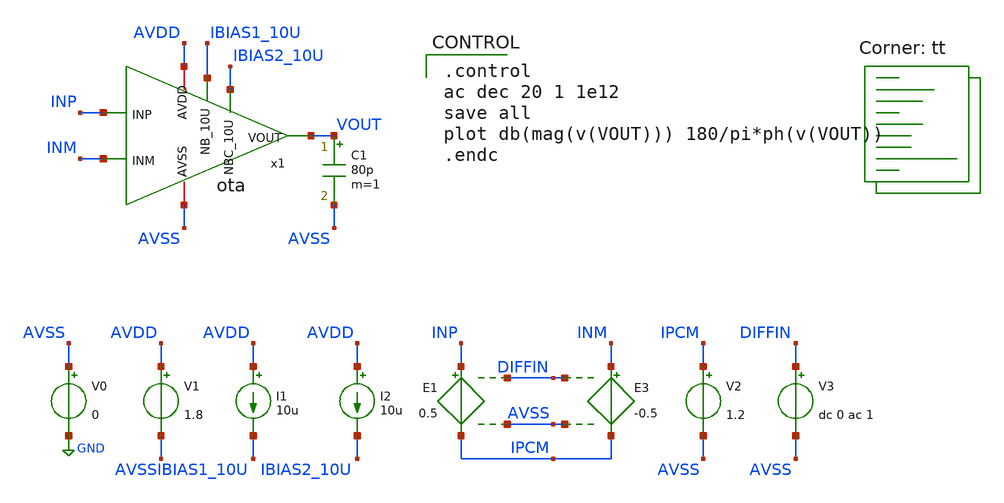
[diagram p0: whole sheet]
** sch_path: ISSCC25/submitted_notebooks/analog_vibes/sim_sch/xschem/tb_ac.sch
**.subckt tb_ac
V0 AVSS GND 0
V1 AVDD AVSS 1.8
I1 AVDD IBIAS1_10U 10u
I2 AVDD IBIAS2_10U 10u
E1 INP IPCM DIFFIN AVSS 0.5
E3 INM IPCM DIFFIN AVSS -0.5
V2 IPCM AVSS 1.2
V3 DIFFIN AVSS dc 0 ac 1
C1 VOUT AVSS 80p m=1
x1 AVDD AVSS INP INM IBIAS1_10U IBIAS2_10U VOUT ota
**** begin user architecture code
.lib $::SKYWATER_MODELS/sky130.lib.spice tt

.control
ac dec 20 1 1e12
save all
plot db(mag(v(VOUT))) 180/pi*ph(v(VOUT))
.endc

**** end user architecture code
**.ends
.GLOBAL GND
.end
